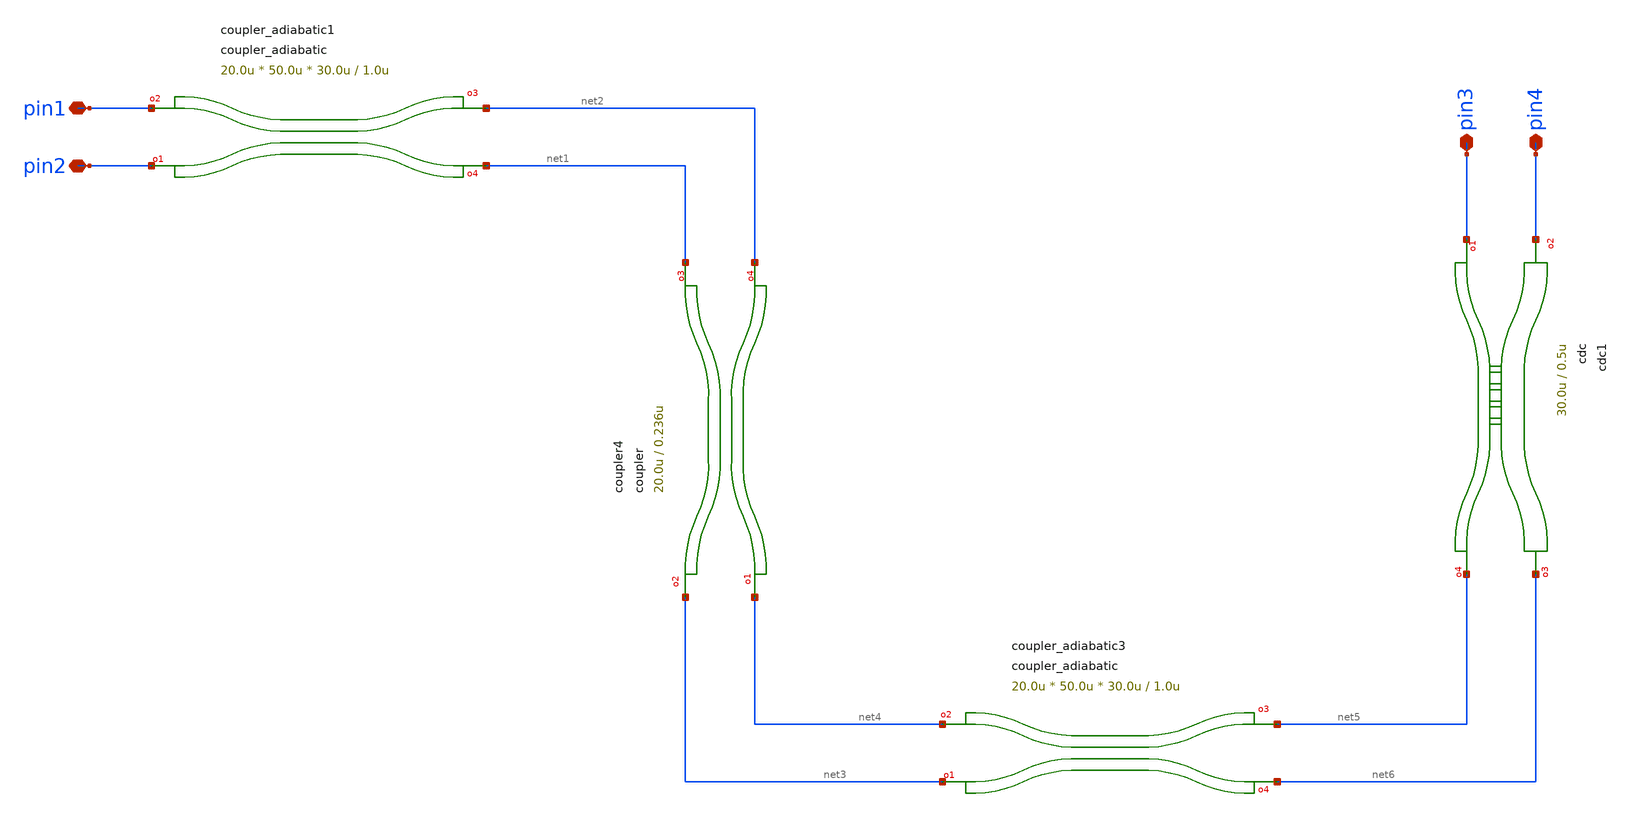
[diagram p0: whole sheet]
** sch_path: xschem/tests/test_sch/test_coupler_adiabatic.sch
* Copyright (c) 2024, Mabrains LLC
* Licensed under the GNU Lesser General Public License, Version 3.0 (the "License");
* you may not use this file except in compliance with the License.
* GNU Lesser General Public License
* Version 3, 29 June 2007
* This program is free software: you can redistribute it and/or modify
* it under the terms of the GNU Lesser General Public License as published
* by the Free Software Foundation, either version 3 of the License, or
* (at your option) any later version.
* This program is distributed in the hope that it will be useful,
* but WITHOUT ANY WARRANTY; without even the implied warranty of
* MERCHANTABILITY or FITNESS FOR A PARTICULAR PURPOSE.  See the
* GNU Lesser General Public License for more details.
* You should have received a copy of the GNU Lesser General Public License
* along with this program.  If not, see <https://www.gnu.org/licenses/>.
* SPDX-License-Identifier: LGPL-3.0
**.subckt test_coupler_adiabatic pin1 pin2 pin3 pin4
*.iopin pin1
*.iopin pin2
*.iopin pin3
*.iopin pin4
Pcoupler_adiabatic1 pin1 pin2 net1 net2 coupler_adiabatic length1=20.0u length2=50.0u length3=30.0u
+ wg_sep=1.0u input_wg_sep=3.0u output_wg_sep=3.0u dw=0.1u
Pcoupler_adiabatic3 net4 net3 net6 net5 coupler_adiabatic length1=20.0u length2=50.0u length3=30.0u
+ wg_sep=1.0u input_wg_sep=3.0u output_wg_sep=3.0u dw=0.1u
Pcoupler4 net3 net4 net1 net2 coupler length=20.0u gap=0.236u dx=10u dy=4.0u
Pcdc1 pin4 pin3 net6 net5 cdc length=30.0u gap=0.5u period=0.22 duty_cycle=0.5 width_top=2.0u
+ width_bot=0.75u dx=10u dy=1.8u
**.ends
.end
